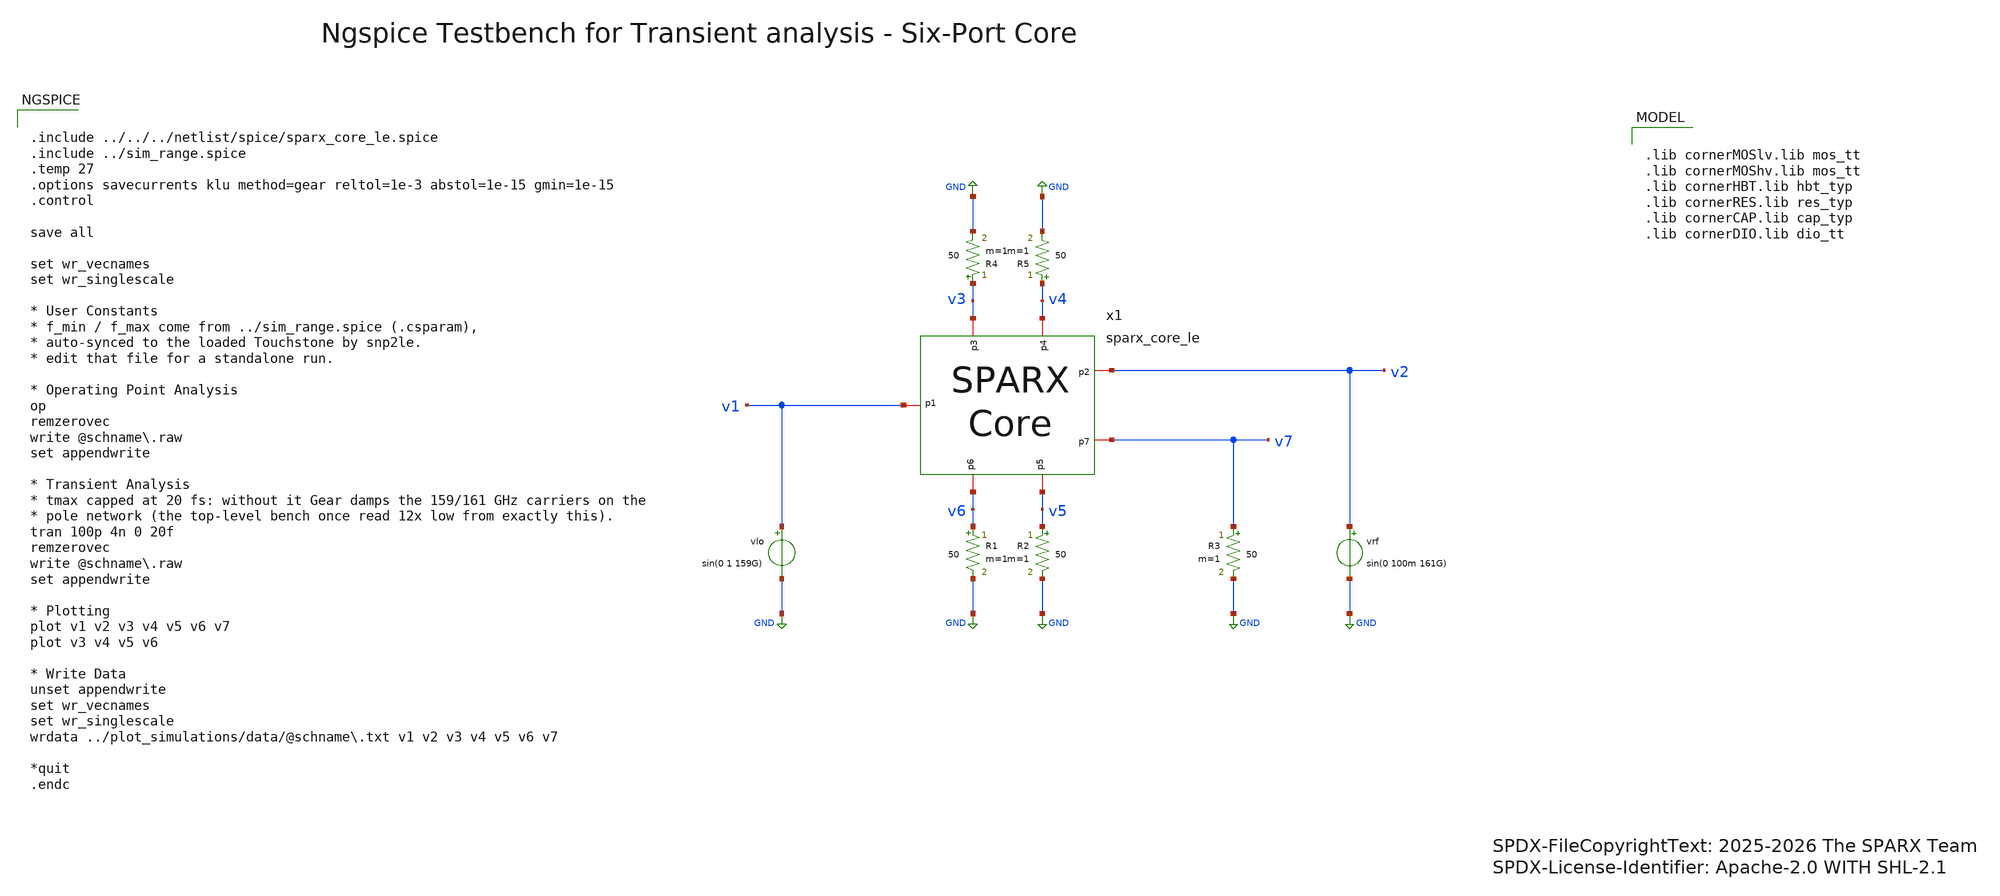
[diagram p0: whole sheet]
** sch_path: testbenches/xschem/sparx_core_le_tb_tran_ngspice.sch
* SPDX-FileCopyrightText: 2025-2026 The SPARX Team
* SPDX-License-Identifier: Apache-2.0 WITH SHL-2.1
**.subckt sparx_core_le_tb_tran_ngspice
vlo v1 GND sin(0 1 159G)
R1 v6 GND 50 m=1
vrf v2 GND sin(0 100m 161G)
R2 v5 GND 50 m=1
R3 v7 GND 50 m=1
R4 v3 GND 50 m=1
R5 v4 GND 50 m=1
x1 v3 v4 v2 v1 v7 v5 v6 sparx_core_le
**** begin user architecture code


.include ../../../netlist/spice/sparx_core_le.spice
.include ../sim_range.spice
.temp 27
.options savecurrents klu method=gear reltol=1e-3 abstol=1e-15 gmin=1e-15
.control

save all

set wr_vecnames
set wr_singlescale

* User Constants
* f_min / f_max come from ../sim_range.spice (.csparam),
* auto-synced to the loaded Touchstone by snp2le.
* edit that file for a standalone run.

* Operating Point Analysis
op
remzerovec
write @schname\.raw
set appendwrite

* Transient Analysis
* tmax capped at 20 fs: without it Gear damps the 159/161 GHz carriers on the
* pole network (the top-level bench once read 12x low from exactly this).
tran 100p 4n 0 20f
remzerovec
write @schname\.raw
set appendwrite

* Plotting
plot v1 v2 v3 v4 v5 v6 v7
plot v3 v4 v5 v6

* Write Data
unset appendwrite
set wr_vecnames
set wr_singlescale
wrdata ../plot_simulations/data/@schname\.txt v1 v2 v3 v4 v5 v6 v7

*quit
.endc



.lib cornerMOSlv.lib mos_tt
.lib cornerMOShv.lib mos_tt
.lib cornerHBT.lib hbt_typ
.lib cornerRES.lib res_typ
.lib cornerCAP.lib cap_typ
.lib cornerDIO.lib dio_tt

**** end user architecture code
**.ends
.GLOBAL GND
.end
